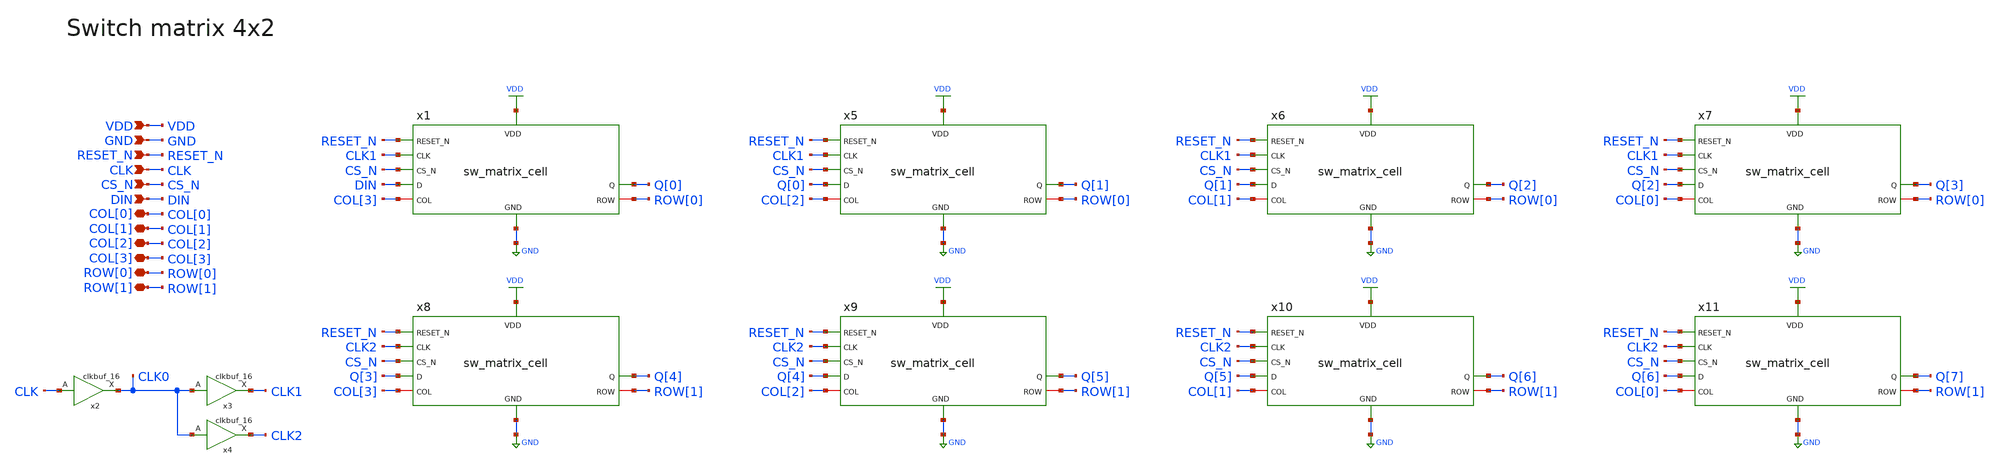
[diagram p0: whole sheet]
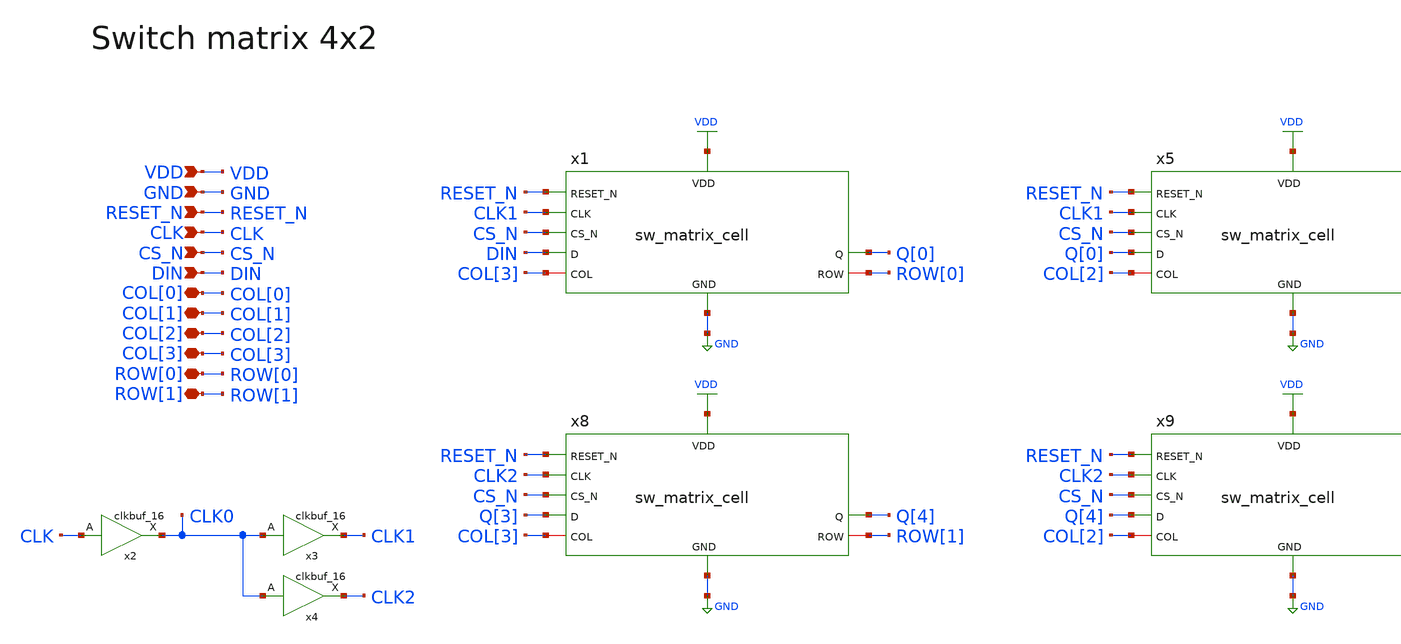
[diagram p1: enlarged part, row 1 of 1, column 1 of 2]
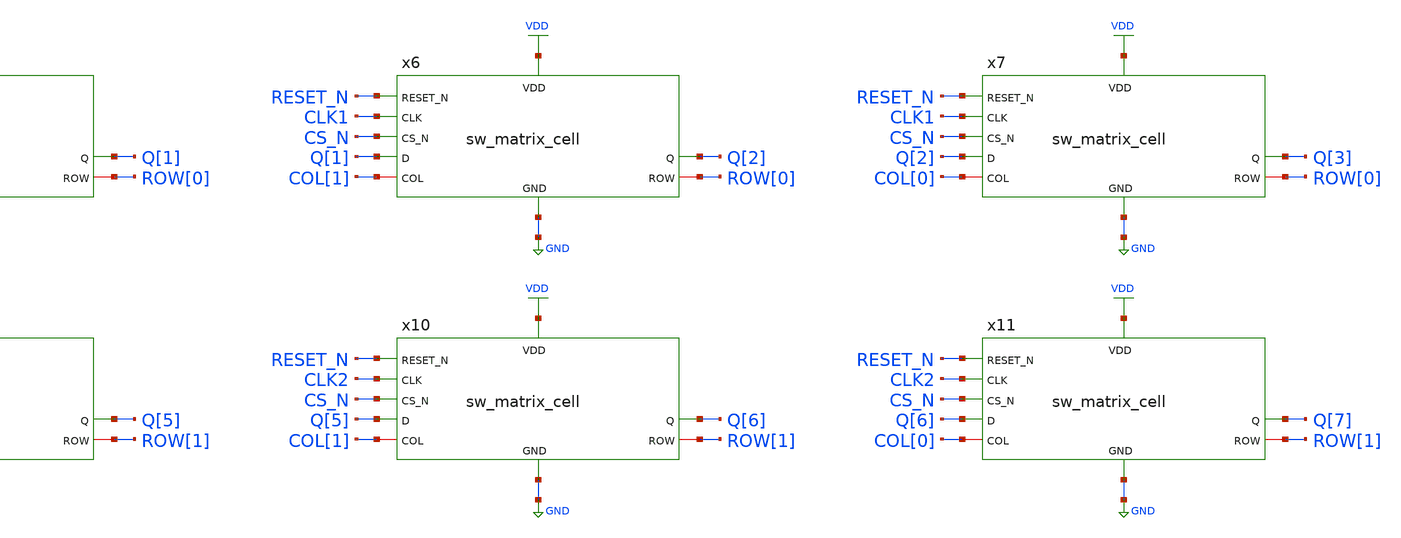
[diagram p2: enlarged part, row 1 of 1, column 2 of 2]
** sch_path: designs/libs/core_analog/sw_matrix/sw_matrix_4x2.sch
* Copyright 2022 GlobalFoundries PDK Authors
* Licensed under the Apache License, Version 2.0 (the "License");
* you may not use this file except in compliance with the License.
* You may obtain a copy of the License at
* https://www.apache.org/licenses/LICENSE-2.0
* Unless required by applicable law or agreed to in writing, software
* distributed under the License is distributed on an "AS IS" BASIS,
* WITHOUT WARRANTIES OR CONDITIONS OF ANY KIND, either express or implied.
* See the License for the specific language governing permissions and
* limitations under the License.
**.subckt sw_matrix_4x2 VDD GND RESET_N CLK CS_N DIN COL[0] COL[1] COL[2] COL[3] ROW[0] ROW[1]
*.ipin VDD
*.ipin GND
*.ipin RESET_N
*.ipin CLK
*.ipin CS_N
*.ipin DIN
*.iopin COL[0]
*.iopin COL[1]
*.iopin COL[2]
*.iopin COL[3]
*.iopin ROW[0]
*.iopin ROW[1]
x1 VDD GND RESET_N CLK1 DIN CS_N Q[0] COL[3] ROW[0] sw_matrix_cell
x5 VDD GND RESET_N CLK1 Q[0] CS_N Q[1] COL[2] ROW[0] sw_matrix_cell
x6 VDD GND RESET_N CLK1 Q[1] CS_N Q[2] COL[1] ROW[0] sw_matrix_cell
x7 VDD GND RESET_N CLK1 Q[2] CS_N Q[3] COL[0] ROW[0] sw_matrix_cell
x8 VDD GND RESET_N CLK2 Q[3] CS_N Q[4] COL[3] ROW[1] sw_matrix_cell
x9 VDD GND RESET_N CLK2 Q[4] CS_N Q[5] COL[2] ROW[1] sw_matrix_cell
x10 VDD GND RESET_N CLK2 Q[5] CS_N Q[6] COL[1] ROW[1] sw_matrix_cell
x11 VDD GND RESET_N CLK2 Q[6] CS_N Q[7] COL[0] ROW[1] sw_matrix_cell
x2 CLK CLK0 VDD VDD GND GND gf180mcu_fd_sc_mcu7t5v0__clkbuf_16
x3 CLK0 CLK1 VDD VDD GND GND gf180mcu_fd_sc_mcu7t5v0__clkbuf_16
x4 CLK0 CLK2 VDD VDD GND GND gf180mcu_fd_sc_mcu7t5v0__clkbuf_16
**.ends
.GLOBAL GND
.GLOBAL VDD
.end
